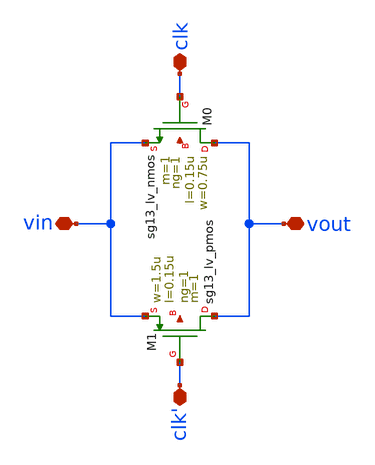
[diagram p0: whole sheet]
** sch_path: design/blocks/transmissiongate/transmissiongate.sch
**.subckt transmissiongate vout vin clk clk'
*.iopin vout
*.iopin vin
*.iopin clk
*.iopin clk'
XM1 vout clk' vin net1 sg13_lv_pmos w=1.5u l=0.15u ng=1 m=1 mm_ok=1
XM0 vout clk vin net2 sg13_lv_nmos w=0.75u l=0.15u ng=1 m=1 mm_ok=1
**.ends
.end
